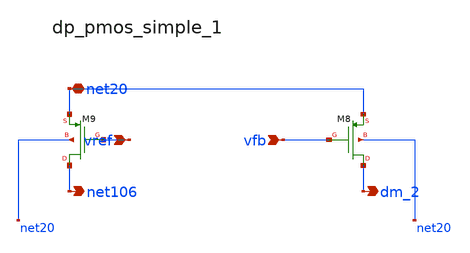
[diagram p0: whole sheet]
** sch_path: analog-db/raw/ldo_001_analoggym_basic/hier/blocks/dp_pmos_simple_1.sch
**.subckt dp_pmos_simple_1 vref vfb net20 net106 dm_2
*.ipin vref
*.ipin vfb
*.iopin net20
*.opin net106
*.opin dm_2
XM8 dm_2 vfb net20 net20 sg13_lv_pmos w=x_dut_xm8_w l=x_dut_xm8_l ng=1 m=x_dut_xm8_m
XM9 net106 vref net20 net20 sg13_lv_pmos w=x_dut_xm9_w l=x_dut_xm9_l ng=1 m=x_dut_xm9_m
**.ends
.end
